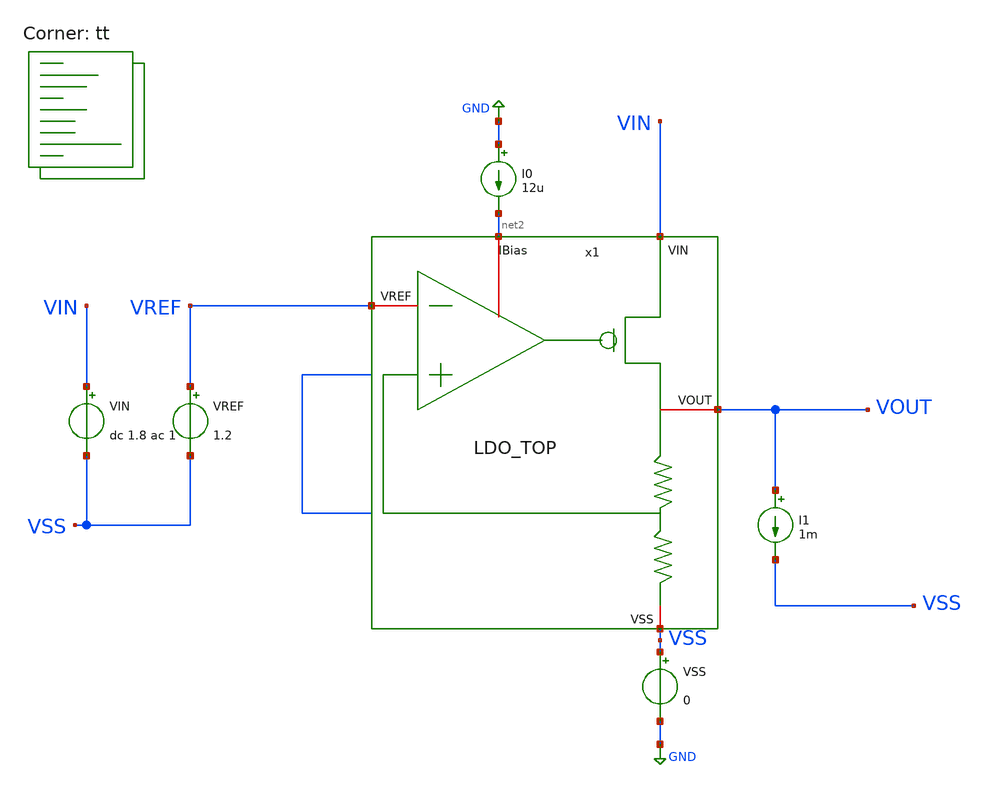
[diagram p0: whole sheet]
** sch_path: LDO_1p5V/tests/PSRR.sch
**.subckt PSRR
VSS VSS GND 0
VREF VREF VSS 1.2
VIN VIN VSS dc 1.8 ac 1
I0 GND net2 12u
I1 VOUT VSS 1m
x1 VIN net2 VREF VOUT VSS LDO_TOP
**** begin user architecture code


.options savecurrents
.save all
.save v(x1.vgate)

.control
set filetype=ascii

echo ===== PSRR ANALYSIS - TWO LOAD CONDITIONS =====

****************************************************
* CASE 1: ILOAD = 10uA
****************************************************

echo ===== CASE 1: ILOAD = 10uA =====

alter I1 10u

op
ac dec 200 1 100G

let vin_ac = v(VIN)
let vout_ac = v(VOUT)
let vgate_ac = v(x1.vgate)

let psrr_gain = mag(vout_ac/vin_ac)
let psrr_10u_db = 20*log10(psrr_gain)

let vin_to_vgate_10u_db = 20*log10(mag(vgate_ac/vin_ac))

meas ac psrr_10u_10Hz   find psrr_10u_db at=10
meas ac psrr_10u_100khz find psrr_10u_db at=100k
meas ac psrr_10u_1mhz   find psrr_10u_db at=1Meg
meas ac psrr_10u_10mhz  find psrr_10u_db at=10Meg
meas ac psrr_10u_max    max psrr_10u_db

echo ===== PSRR RESULTS - ILOAD = 10uA =====
print psrr_10u_10Hz
print psrr_10u_100khz
print psrr_10u_1mhz
print psrr_10u_10mhz
print psrr_10u_max


****************************************************
* CASE 2: ILOAD = 1mA
****************************************************

echo ===== CASE 2: ILOAD = 1mA =====

alter I1 1m

op
ac dec 200 1 10G

let vin_ac = v(VIN)
let vout_ac = v(VOUT)
let vgate_ac = v(x1.vgate)

let psrr_gain = mag(vout_ac/vin_ac)
let psrr_1m_db = 20*log10(psrr_gain)

let vin_to_vgate_1m_db = 20*log10(mag(vgate_ac/vin_ac))

meas ac psrr_1m_10hz   find psrr_1m_db at=10
meas ac psrr_1m_100khz find psrr_1m_db at=100k
meas ac psrr_1m_1mhz   find psrr_1m_db at=1Meg
meas ac psrr_1m_10mhz  find psrr_1m_db at=10Meg
meas ac psrr_1m_max    max psrr_1m_db

echo ===== PSRR RESULTS - ILOAD = 1mA =====

print psrr_1m_10hz
print psrr_1m_100khz
print psrr_1m_1mhz
print psrr_1m_10mhz
print psrr_1m_max


****************************************************
* PLOT BOTH LOAD CONDITIONS IN ONE GRAPH
****************************************************

echo ===== PLOTTING BOTH LOAD CONDITIONS =====

plot ac1.psrr_10u_db ac2.psrr_1m_db

plot ac1.vin_to_vgate_10u_db ac2.vin_to_vgate_1m_db

*plot ac1.psrr_10u_db ac2.psrr_1m_db ac1.vin_to_vgate_10u_db ac2.vin_to_vgate_1m_db

.endc


.lib $::SKYWATER_MODELS/sky130.lib.spice tt
**** end user architecture code
**.ends

* expanding   symbol:  /foss/designs/Curso_Semiconductores/LDO_1p5V/schematics/LDO_TOP.sym # of
*+ pins=5
** sym_path: LDO/LDO_TOP.sym
** sch_path: LDO/LDO_TOP.sch
.subckt LDO_TOP VIN IBias VREF VOUT VSS
*.iopin VIN
*.iopin VREF
*.iopin IBias
*.iopin VOUT
*.iopin VSS
x1 VIN IBias VREF VOUT net1 net1 VSS LDO
.ends


* expanding   symbol:  /foss/designs/Curso_Semiconductores/LDO/LDO.sym # of pins=7
** sym_path: LDO/LDO.sym
** sch_path: LDO/LDO.sch
.subckt LDO VIN IBias VREF VOUT VFB1 VFB2 VSS
*.iopin VIN
*.iopin VREF
*.iopin VFB1
*.iopin VSS
*.iopin VFB2
*.iopin VOUT
*.iopin IBias
XM7 VOUT Vgate VIN VIN sky130_fd_pr__pfet_01v8 L=0.15 W=6 nf=1 ad='int((1 + 1)/2) * 6 / 1 * 0.29' as='int((1 + 2)/2) * 6 / 1 * 0.29'
+ pd='2*int((1 + 1)/2) * (6 / 1 + 0.29)' ps='2*int((1 + 2)/2) * (6 / 1 + 0.29)' nrd='0.29 / 6 ' nrs='0.29 / 6 '
+ sa=0 sb=0 sd=0 mult=50 m=50
XC3 Vgate VOUT sky130_fd_pr__model__cap_mim W=10 L=10 MF=1 m=1
x1 VIN Vgate VREF VFB1 IBias VSS OTA_5T
x2 VOUT VFB2 VSS RES_FB
.ends


* expanding   symbol:  /foss/designs/Curso_Semiconductores/OTA_5T/OTA_5T.sym # of pins=6
** sym_path: /foss/designs/Curso_Semiconductores/OTA_5T/OTA_5T.sym
** sch_path: /foss/designs/Curso_Semiconductores/OTA_5T/OTA_5T.sch
.subckt OTA_5T VIN VOUT_AMP VINN VINP IB VSS
*.iopin VIN
*.iopin VSS
*.iopin VOUT_AMP
*.iopin IB
*.iopin VINN
*.iopin VINP
XM1 IB IB VSS VSS sky130_fd_pr__nfet_01v8 L=1 W=2.5 nf=1 ad='int((1 + 1)/2) * 2.5 / 1 * 0.29' as='int((1 + 2)/2) * 2.5 / 1 * 0.29'
+ pd='2*int((1 + 1)/2) * (2.5 / 1 + 0.29)' ps='2*int((1 + 2)/2) * (2.5 / 1 + 0.29)' nrd='0.29 / 2.5 ' nrs='0.29 / 2.5 '
+ sa=0 sb=0 sd=0 mult=4 m=4
XM2 tail IB VSS VSS sky130_fd_pr__nfet_01v8 L=1 W=2.5 nf=1 ad='int((1 + 1)/2) * 2.5 / 1 * 0.29' as='int((1 + 2)/2) * 2.5 / 1 * 0.29'
+ pd='2*int((1 + 1)/2) * (2.5 / 1 + 0.29)' ps='2*int((1 + 2)/2) * (2.5 / 1 + 0.29)' nrd='0.29 / 2.5 ' nrs='0.29 / 2.5 '
+ sa=0 sb=0 sd=0 mult=4 m=4
XM3 net1 VINP tail VSS sky130_fd_pr__nfet_01v8 L=1 W=3 nf=1 ad='int((1 + 1)/2) * 3 / 1 * 0.29' as='int((1 + 2)/2) * 3 / 1 * 0.29'
+ pd='2*int((1 + 1)/2) * (3 / 1 + 0.29)' ps='2*int((1 + 2)/2) * (3 / 1 + 0.29)' nrd='0.29 / 3 ' nrs='0.29 / 3 '
+ sa=0 sb=0 sd=0 mult=4 m=4
XM4 VOUT_AMP VINN tail VSS sky130_fd_pr__nfet_01v8 L=1 W=3 nf=1 ad='int((1 + 1)/2) * 3 / 1 * 0.29' as='int((1 + 2)/2) * 3 / 1 * 0.29'
+ pd='2*int((1 + 1)/2) * (3 / 1 + 0.29)' ps='2*int((1 + 2)/2) * (3 / 1 + 0.29)' nrd='0.29 / 3 ' nrs='0.29 / 3 '
+ sa=0 sb=0 sd=0 mult=4 m=4
XM5 VOUT_AMP net1 VIN VIN sky130_fd_pr__pfet_01v8 L=1 W=6 nf=1 ad='int((1 + 1)/2) * 6 / 1 * 0.29' as='int((1 + 2)/2) * 6 / 1 * 0.29'
+ pd='2*int((1 + 1)/2) * (6 / 1 + 0.29)' ps='2*int((1 + 2)/2) * (6 / 1 + 0.29)' nrd='0.29 / 6 ' nrs='0.29 / 6 '
+ sa=0 sb=0 sd=0 mult=4 m=4
XM6 net1 net1 VIN VIN sky130_fd_pr__pfet_01v8 L=1 W=6 nf=1 ad='int((1 + 1)/2) * 6 / 1 * 0.29' as='int((1 + 2)/2) * 6 / 1 * 0.29'
+ pd='2*int((1 + 1)/2) * (6 / 1 + 0.29)' ps='2*int((1 + 2)/2) * (6 / 1 + 0.29)' nrd='0.29 / 6 ' nrs='0.29 / 6 '
+ sa=0 sb=0 sd=0 mult=4 m=4
XD tail VSS tail VSS sky130_fd_pr__nfet_01v8 L=0.15 W=3 nf=1 ad='int((1 + 1)/2) * 3 / 1 * 0.29' as='int((1 + 2)/2) * 3 / 1 * 0.29'
+ pd='2*int((1 + 1)/2) * (3 / 1 + 0.29)' ps='2*int((1 + 2)/2) * (3 / 1 + 0.29)' nrd='0.29 / 3 ' nrs='0.29 / 3 '
+ sa=0 sb=0 sd=0 mult=4 m=4
XM7 VIN VIN VIN VIN sky130_fd_pr__pfet_01v8 L=0.15 W=6 nf=1 ad='int((1 + 1)/2) * 6 / 1 * 0.29' as='int((1 + 2)/2) * 6 / 1 * 0.29'
+ pd='2*int((1 + 1)/2) * (6 / 1 + 0.29)' ps='2*int((1 + 2)/2) * (6 / 1 + 0.29)' nrd='0.29 / 6 ' nrs='0.29 / 6 '
+ sa=0 sb=0 sd=0 mult=4 m=4
.ends


* expanding   symbol:  /foss/designs/Curso_Semiconductores/RES_FB/RES_FB.sym # of pins=3
** sym_path: RES_FB/RES_FB.sym
** sch_path: RES_FB/RES_FB.sch
.subckt RES_FB VOUT VFB VSS
*.iopin VOUT
*.iopin VFB
*.iopin VSS
XR11 net1 VOUT VSS sky130_fd_pr__res_xhigh_po_0p69 L=8.62 mult=1 m=1
XR1 VFB net1 VSS sky130_fd_pr__res_xhigh_po_0p69 L=8.62 mult=1 m=1
XR2 net8 VFB VSS sky130_fd_pr__res_xhigh_po_0p69 L=8.62 mult=1 m=1
XR3 net4 net8 VSS sky130_fd_pr__res_xhigh_po_0p69 L=8.62 mult=1 m=1
XR4 net2 net4 VSS sky130_fd_pr__res_xhigh_po_0p69 L=8.62 mult=1 m=1
XR5 net5 net2 VSS sky130_fd_pr__res_xhigh_po_0p69 L=8.62 mult=1 m=1
XR6 net3 net5 VSS sky130_fd_pr__res_xhigh_po_0p69 L=8.62 mult=1 m=1
XR7 net7 net3 VSS sky130_fd_pr__res_xhigh_po_0p69 L=8.62 mult=1 m=1
XR8 net6 net7 VSS sky130_fd_pr__res_xhigh_po_0p69 L=8.62 mult=1 m=1
XR9 VSS net6 VSS sky130_fd_pr__res_xhigh_po_0p69 L=8.62 mult=1 m=1
.ends

.GLOBAL GND
.end
